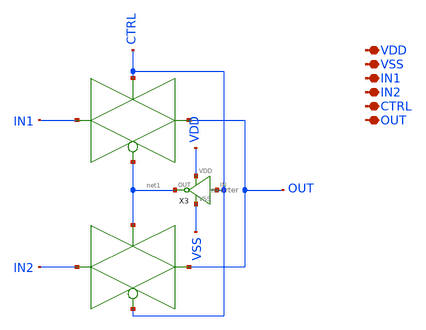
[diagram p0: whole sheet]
** sch_path: xschem/MISC/MUX/MUX.sch
**.subckt MUX VDD VSS IN1 IN2 CTRL OUT
*.iopin VDD
*.iopin VSS
*.iopin IN1
*.iopin IN2
*.iopin CTRL
*.iopin OUT
X3 CTRL VSS net1 VDD inverter
**.ends
.end
